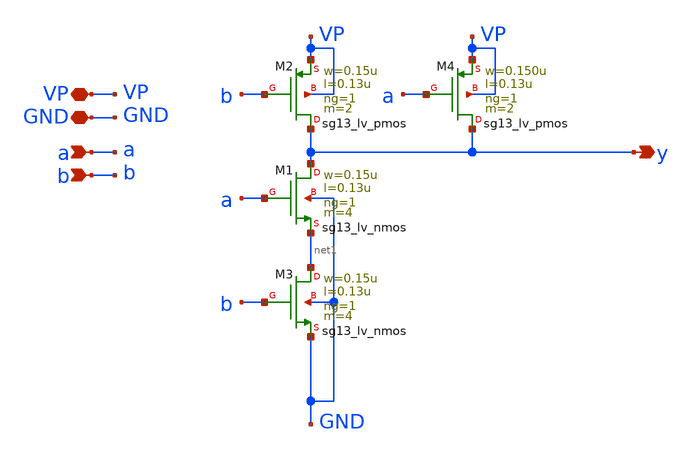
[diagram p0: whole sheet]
** sch_path: schematics/divider/schematics/NAND_2in_x2.sch
**.subckt NAND_2in_x2 y GND a VP b
*.opin y
*.iopin GND
*.ipin a
*.iopin VP
*.ipin b
XM1 y a net1 GND sg13_lv_nmos w=0.15u l=0.13u ng=1 m=4 mm_ok=1
XM3 net1 b GND GND sg13_lv_nmos w=0.15u l=0.13u ng=1 m=4 mm_ok=1
XM2 y b VP VP sg13_lv_pmos w=0.15u l=0.13u ng=1 m=2 mm_ok=1
XM4 y a VP VP sg13_lv_pmos w=0.150u l=0.13u ng=1 m=2 mm_ok=1
**.ends
.end
